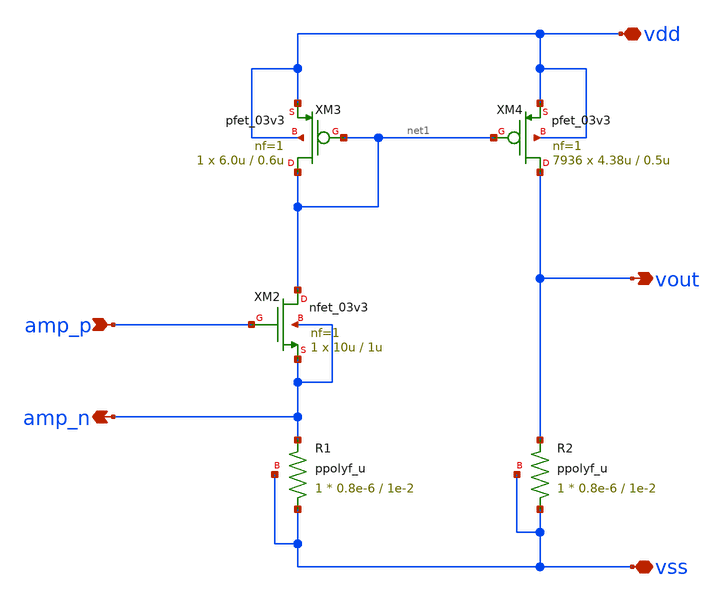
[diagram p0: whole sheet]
** sch_path: submit_version/xschem/ldo_currentmirror.sch
**.subckt ldo_currentmirror vdd vss vout amp_p amp_n
*.iopin vdd
*.iopin vss
*.opin vout
*.ipin amp_p
*.opin amp_n
XM3 net1 net1 vdd vdd pfet_03v3 L=0.6u W=6.0u nf=1 ad='int((nf+1)/2) * W/nf * 0.18u' as='int((nf+2)/2) * W/nf * 0.18u'
+ pd='2*int((nf+1)/2) * (W/nf + 0.18u)' ps='2*int((nf+2)/2) * (W/nf + 0.18u)' nrd='0.18u / W' nrs='0.18u / W'
+ sa=0 sb=0 sd=0 m=1
XM4 vout net1 vdd vdd pfet_03v3 L=0.5u W=4.38u nf=1 ad='int((nf+1)/2) * W/nf * 0.18u' as='int((nf+2)/2) * W/nf * 0.18u'
+ pd='2*int((nf+1)/2) * (W/nf + 0.18u)' ps='2*int((nf+2)/2) * (W/nf + 0.18u)' nrd='0.18u / W' nrs='0.18u / W'
+ sa=0 sb=0 sd=0 m=7936
XR1 vss amp_n vss ppolyf_u r_width=0.8e-6 r_length=1e-2 m=1
XM2 net1 amp_p amp_n amp_n nfet_03v3 L=1u W=10u nf=1 ad='int((nf+1)/2) * W/nf * 0.18u' as='int((nf+2)/2) * W/nf * 0.18u'
+ pd='2*int((nf+1)/2) * (W/nf + 0.18u)' ps='2*int((nf+2)/2) * (W/nf + 0.18u)' nrd='0.18u / W' nrs='0.18u / W'
+ sa=0 sb=0 sd=0 m=1
XR2 vss vout vss ppolyf_u r_width=0.8e-6 r_length=1e-2 m=1
**.ends
.end
